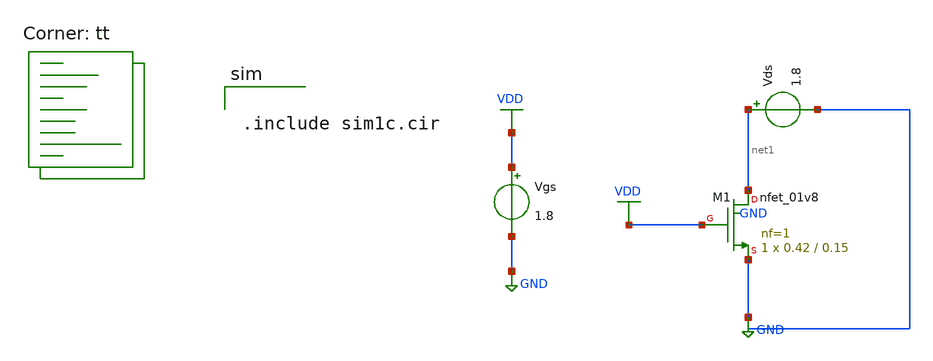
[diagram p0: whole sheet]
** sch_path: assignments/assignment1/assign1c.sch
**.subckt assign1c
XM1 net1 VDD GND GND sky130_fd_pr__nfet_01v8 L=0.15 W=0.42 nf=1 ad='int((nf+1)/2) * W/nf * 0.29' as='int((nf+2)/2) * W/nf * 0.29'
+ pd='2*int((nf+1)/2) * (W/nf + 0.29)' ps='2*int((nf+2)/2) * (W/nf + 0.29)' nrd='0.29 / W' nrs='0.29 / W'
+ sa=0 sb=0 sd=0 mult=1 m=1
Vds net1 GND 1.8
Vgs VDD GND 1.8
**** begin user architecture code


.include sim1c.cir


.lib $::SKYWATER_MODELS/sky130.lib.spice tt
**** end user architecture code
**.ends
.GLOBAL GND
.GLOBAL VDD
.end
